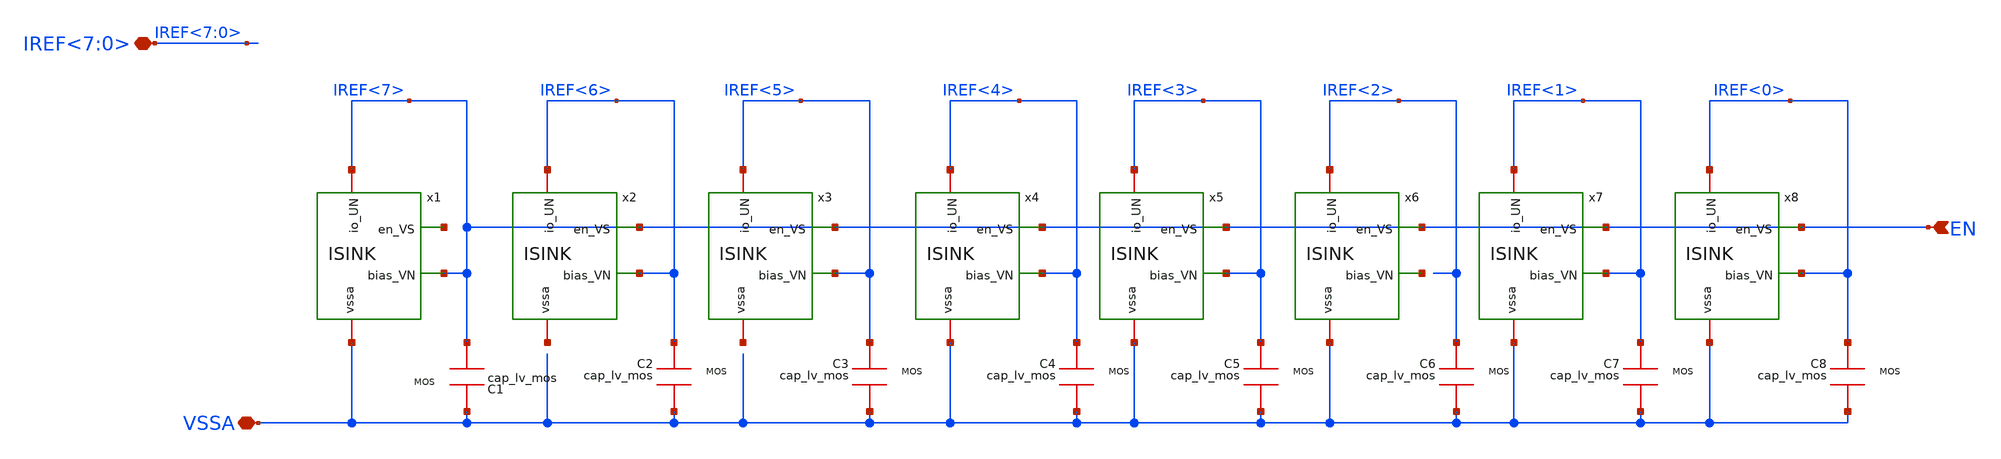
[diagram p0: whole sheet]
** sch_path: CoreDiodeT.sch
**.subckt CoreDiodeT VSSA EN IREF<7:0>
*.iopin VSSA
*.ipin EN
*.iopin IREF<7:0>
x1 EN VSSA net1 EN ISINK
x2 IREF<6> net2 EN IREF<6> ISINK
x3 IREF<5> net3 EN IREF<5> ISINK
x4 IREF<4> VSSA EN IREF<4> ISINK
x5 IREF<3> VSSA EN IREF<3> ISINK
x6 net4 VSSA EN IREF<2> ISINK
x7 IREF<1> VSSA EN IREF<1> ISINK
x8 IREF<0> VSSA EN IREF<0> ISINK
C1 sg13_lv_nmos w=14e-6 l=13e-6 ng=1 m=1
C2 sg13_lv_nmos w=14e-6 l=13e-6 ng=1 m=1
C3 sg13_lv_nmos w=14e-6 l=13e-6 ng=1 m=1
C4 sg13_lv_nmos w=14e-6 l=13e-6 ng=1 m=1
C5 sg13_lv_nmos w=14e-6 l=13e-6 ng=1 m=1
C6 sg13_lv_nmos w=14e-6 l=13e-6 ng=1 m=1
C7 sg13_lv_nmos w=14e-6 l=13e-6 ng=1 m=1
C8 sg13_lv_nmos w=14e-6 l=13e-6 ng=1 m=1
**.ends
.end
